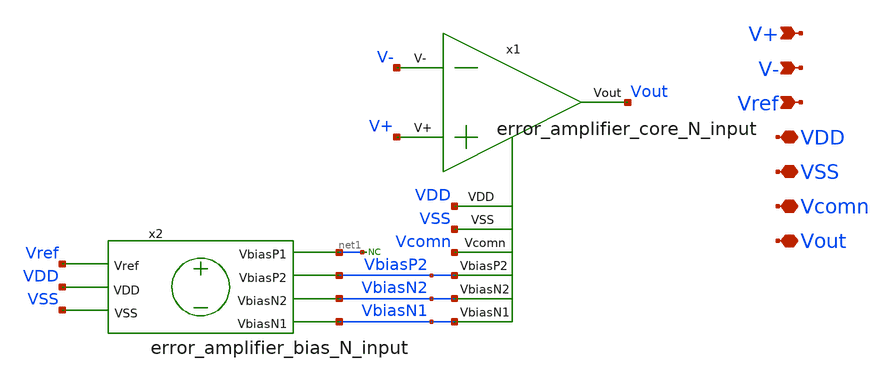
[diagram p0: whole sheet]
** sch_path: blocks/composite/folded_cascode/designs/gf180/error_amplifier_N_input/xschem/error_amplifier_N_input.sch
**.subckt error_amplifier_N_input V+ Vout V- Vref VDD VSS Vcomn
*.ipin V+
*.iopin Vout
*.ipin V-
*.ipin Vref
*.iopin VDD
*.iopin VSS
*.iopin Vcomn
x1 VbiasP2 VbiasN2 VbiasN1 Vout V+ V- VDD VSS Vcomn error_amplifier_core_N_input
x2 VbiasN1 VbiasN2 VbiasP2 VDD VSS Vref net1 error_amplifier_bias_N_input
* noconn #net1
**.ends

* expanding   symbol:  error_amplifier_core_N_input.sym # of pins=9
** sym_path: blocks/composite/folded_cascode/designs/gf180/error_amplifier_core_N_input/xschem/error_amplifier_core_N_input.sym
** sch_path: blocks/composite/folded_cascode/designs/gf180/error_amplifier_core_N_input/xschem/error_amplifier_core_N_input.sch
.subckt error_amplifier_core_N_input VbiasP2 VbiasN2 VbiasN1 Vout V+ V- VDD VSS Vcomn
*.ipin VbiasN2
*.iopin VDD
*.ipin VbiasP2
*.ipin VbiasN1
*.ipin V+
*.ipin V-
*.iopin VSS
*.iopin Vcomn
*.iopin Vout
XM4 Vdm6 Val VDD VDD pfet_03v3 L=0.3u W=4u nf=1 ad='int((nf+1)/2) * W/nf * 0.18u' as='int((nf+2)/2) * W/nf * 0.18u'
+ pd='2*int((nf+1)/2) * (W/nf + 0.18u)' ps='2*int((nf+2)/2) * (W/nf + 0.18u)' nrd='0.18u / W' nrs='0.18u / W'
+ sa=0 sb=0 sd=0 m=12
XM3 Vdm5 Val VDD VDD pfet_03v3 L=0.3u W=4u nf=1 ad='int((nf+1)/2) * W/nf * 0.18u' as='int((nf+2)/2) * W/nf * 0.18u'
+ pd='2*int((nf+1)/2) * (W/nf + 0.18u)' ps='2*int((nf+2)/2) * (W/nf + 0.18u)' nrd='0.18u / W' nrs='0.18u / W'
+ sa=0 sb=0 sd=0 m=12
XM5 Val VbiasP2 Vdm5 VDD pfet_03v3 L=2u W=6u nf=1 ad='int((nf+1)/2) * W/nf * 0.18u' as='int((nf+2)/2) * W/nf * 0.18u'
+ pd='2*int((nf+1)/2) * (W/nf + 0.18u)' ps='2*int((nf+2)/2) * (W/nf + 0.18u)' nrd='0.18u / W' nrs='0.18u / W'
+ sa=0 sb=0 sd=0 m=2
XM6 Vout VbiasP2 Vdm6 VDD pfet_03v3 L=2u W=6u nf=1 ad='int((nf+1)/2) * W/nf * 0.18u' as='int((nf+2)/2) * W/nf * 0.18u'
+ pd='2*int((nf+1)/2) * (W/nf + 0.18u)' ps='2*int((nf+2)/2) * (W/nf + 0.18u)' nrd='0.18u / W' nrs='0.18u / W'
+ sa=0 sb=0 sd=0 m=2
XM9 net1 VbiasN1 VSS VSS nfet_03v3 L=2u W=2u nf=1 ad='int((nf+1)/2) * W/nf * 0.18u' as='int((nf+2)/2) * W/nf * 0.18u'
+ pd='2*int((nf+1)/2) * (W/nf + 0.18u)' ps='2*int((nf+2)/2) * (W/nf + 0.18u)' nrd='0.18u / W' nrs='0.18u / W'
+ sa=0 sb=0 sd=0 m=2
XM8 Vout VbiasN2 Vcomn VSS nfet_03v3 L=2u W=5u nf=1 ad='int((nf+1)/2) * W/nf * 0.18u' as='int((nf+2)/2) * W/nf * 0.18u'
+ pd='2*int((nf+1)/2) * (W/nf + 0.18u)' ps='2*int((nf+2)/2) * (W/nf + 0.18u)' nrd='0.18u / W' nrs='0.18u / W'
+ sa=0 sb=0 sd=0 m=1
XM7 Val VbiasN2 net1 VSS nfet_03v3 L=2u W=5u nf=1 ad='int((nf+1)/2) * W/nf * 0.18u' as='int((nf+2)/2) * W/nf * 0.18u'
+ pd='2*int((nf+1)/2) * (W/nf + 0.18u)' ps='2*int((nf+2)/2) * (W/nf + 0.18u)' nrd='0.18u / W' nrs='0.18u / W'
+ sa=0 sb=0 sd=0 m=1
XM10 Vcomn VbiasN1 VSS VSS nfet_03v3 L=2u W=2u nf=1 ad='int((nf+1)/2) * W/nf * 0.18u' as='int((nf+2)/2) * W/nf * 0.18u'
+ pd='2*int((nf+1)/2) * (W/nf + 0.18u)' ps='2*int((nf+2)/2) * (W/nf + 0.18u)' nrd='0.18u / W' nrs='0.18u / W'
+ sa=0 sb=0 sd=0 m=2
XM15 VDD VDD VDD VDD pfet_03v3 L=3u W=1u nf=1 ad='int((nf+1)/2) * W/nf * 0.18u' as='int((nf+2)/2) * W/nf * 0.18u'
+ pd='2*int((nf+1)/2) * (W/nf + 0.18u)' ps='2*int((nf+2)/2) * (W/nf + 0.18u)' nrd='0.18u / W' nrs='0.18u / W'
+ sa=0 sb=0 sd=0 m=28
XM16 VDD VDD VDD VDD pfet_03v3 L=1.5u W=1u nf=1 ad='int((nf+1)/2) * W/nf * 0.18u' as='int((nf+2)/2) * W/nf * 0.18u'
+ pd='2*int((nf+1)/2) * (W/nf + 0.18u)' ps='2*int((nf+2)/2) * (W/nf + 0.18u)' nrd='0.18u / W' nrs='0.18u / W'
+ sa=0 sb=0 sd=0 m=20
XM13 VSS VSS VSS VSS nfet_03v3 L=3u W=1u nf=1 ad='int((nf+1)/2) * W/nf * 0.18u' as='int((nf+2)/2) * W/nf * 0.18u'
+ pd='2*int((nf+1)/2) * (W/nf + 0.18u)' ps='2*int((nf+2)/2) * (W/nf + 0.18u)' nrd='0.18u / W' nrs='0.18u / W'
+ sa=0 sb=0 sd=0 m=18
XM12 VSS VSS VSS VSS nfet_03v3 L=6.5u W=0.5u nf=1 ad='int((nf+1)/2) * W/nf * 0.18u' as='int((nf+2)/2) * W/nf * 0.18u'
+ pd='2*int((nf+1)/2) * (W/nf + 0.18u)' ps='2*int((nf+2)/2) * (W/nf + 0.18u)' nrd='0.18u / W' nrs='0.18u / W'
+ sa=0 sb=0 sd=0 m=36
XM14 VSS VSS VSS VSS nfet_03v3 L=1u W=1u nf=1 ad='int((nf+1)/2) * W/nf * 0.18u' as='int((nf+2)/2) * W/nf * 0.18u'
+ pd='2*int((nf+1)/2) * (W/nf + 0.18u)' ps='2*int((nf+2)/2) * (W/nf + 0.18u)' nrd='0.18u / W' nrs='0.18u / W'
+ sa=0 sb=0 sd=0 m=30
XM1 Vdm6 V- net2 VSS nfet_03v3 L=1u W=10u nf=1 ad='int((nf+1)/2) * W/nf * 0.18u' as='int((nf+2)/2) * W/nf * 0.18u'
+ pd='2*int((nf+1)/2) * (W/nf + 0.18u)' ps='2*int((nf+2)/2) * (W/nf + 0.18u)' nrd='0.18u / W' nrs='0.18u / W'
+ sa=0 sb=0 sd=0 m=20
XM2 Vdm5 V+ net2 VSS nfet_03v3 L=1u W=10u nf=1 ad='int((nf+1)/2) * W/nf * 0.18u' as='int((nf+2)/2) * W/nf * 0.18u'
+ pd='2*int((nf+1)/2) * (W/nf + 0.18u)' ps='2*int((nf+2)/2) * (W/nf + 0.18u)' nrd='0.18u / W' nrs='0.18u / W'
+ sa=0 sb=0 sd=0 m=20
XM11 net2 VbiasN1 VSS VSS nfet_03v3 L=2u W=2u nf=1 ad='int((nf+1)/2) * W/nf * 0.18u' as='int((nf+2)/2) * W/nf * 0.18u'
+ pd='2*int((nf+1)/2) * (W/nf + 0.18u)' ps='2*int((nf+2)/2) * (W/nf + 0.18u)' nrd='0.18u / W' nrs='0.18u / W'
+ sa=0 sb=0 sd=0 m=40
.ends


* expanding   symbol:  error_amplifier_bias_N_input.sym # of pins=7
** sym_path: blocks/composite/folded_cascode/designs/gf180/error_amplifier_bias_N_input/xschem/error_amplifier_bias_N_input.sym
** sch_path: blocks/composite/folded_cascode/designs/gf180/error_amplifier_bias_N_input/xschem/error_amplifier_bias_N_input.sch
.subckt error_amplifier_bias_N_input VbiasN1 VbiasN2 VbiasP2 VDD VSS Vref VbiasP1
*.ipin Vref
*.iopin VbiasN1
*.iopin VbiasN2
*.iopin VDD
*.iopin VbiasP2
*.iopin VSS
*.iopin VbiasP1
XM1 VbiasN2 VbiasN2 net2 VSS nfet_03v3 L=6u W=0.5u nf=1 ad='int((nf+1)/2) * W/nf * 0.18u' as='int((nf+2)/2) * W/nf * 0.18u'
+ pd='2*int((nf+1)/2) * (W/nf + 0.18u)' ps='2*int((nf+2)/2) * (W/nf + 0.18u)' nrd='0.18u / W' nrs='0.18u / W'
+ sa=0 sb=0 sd=0 m=1
XM2 VbiasP1 VbiasP1 VDD VDD pfet_03v3 L=2u W=0.5u nf=1 ad='int((nf+1)/2) * W/nf * 0.18u' as='int((nf+2)/2) * W/nf * 0.18u'
+ pd='2*int((nf+1)/2) * (W/nf + 0.18u)' ps='2*int((nf+2)/2) * (W/nf + 0.18u)' nrd='0.18u / W' nrs='0.18u / W'
+ sa=0 sb=0 sd=0 m=1
XM3 VbiasP1 Vref net1 VSS nfet_03v3 L=6u W=0.5u nf=1 ad='int((nf+1)/2) * W/nf * 0.18u' as='int((nf+2)/2) * W/nf * 0.18u'
+ pd='2*int((nf+1)/2) * (W/nf + 0.18u)' ps='2*int((nf+2)/2) * (W/nf + 0.18u)' nrd='0.18u / W' nrs='0.18u / W'
+ sa=0 sb=0 sd=0 m=1
XM4 VbiasN2 VbiasP1 VDD VDD pfet_03v3 L=2u W=0.5u nf=1 ad='int((nf+1)/2) * W/nf * 0.18u' as='int((nf+2)/2) * W/nf * 0.18u'
+ pd='2*int((nf+1)/2) * (W/nf + 0.18u)' ps='2*int((nf+2)/2) * (W/nf + 0.18u)' nrd='0.18u / W' nrs='0.18u / W'
+ sa=0 sb=0 sd=0 m=1
XM5 VbiasN1 VbiasP1 VDD VDD pfet_03v3 L=2u W=0.5u nf=1 ad='int((nf+1)/2) * W/nf * 0.18u' as='int((nf+2)/2) * W/nf * 0.18u'
+ pd='2*int((nf+1)/2) * (W/nf + 0.18u)' ps='2*int((nf+2)/2) * (W/nf + 0.18u)' nrd='0.18u / W' nrs='0.18u / W'
+ sa=0 sb=0 sd=0 m=1
XM6 net6 VbiasP2 VDD VDD pfet_03v3 L=2u W=0.5u nf=1 ad='int((nf+1)/2) * W/nf * 0.18u' as='int((nf+2)/2) * W/nf * 0.18u'
+ pd='2*int((nf+1)/2) * (W/nf + 0.18u)' ps='2*int((nf+2)/2) * (W/nf + 0.18u)' nrd='0.18u / W' nrs='0.18u / W'
+ sa=0 sb=0 sd=0 m=1
XM7 VbiasP2 VbiasP2 net6 VDD pfet_03v3 L=2u W=0.5u nf=1 ad='int((nf+1)/2) * W/nf * 0.18u' as='int((nf+2)/2) * W/nf * 0.18u'
+ pd='2*int((nf+1)/2) * (W/nf + 0.18u)' ps='2*int((nf+2)/2) * (W/nf + 0.18u)' nrd='0.18u / W' nrs='0.18u / W'
+ sa=0 sb=0 sd=0 m=1
XM8 net7 net8 VDD VDD pfet_03v3 L=2u W=0.5u nf=1 ad='int((nf+1)/2) * W/nf * 0.18u' as='int((nf+2)/2) * W/nf * 0.18u'
+ pd='2*int((nf+1)/2) * (W/nf + 0.18u)' ps='2*int((nf+2)/2) * (W/nf + 0.18u)' nrd='0.18u / W' nrs='0.18u / W'
+ sa=0 sb=0 sd=0 m=3
XM9 net8 VbiasP2 net7 VDD pfet_03v3 L=2u W=0.5u nf=1 ad='int((nf+1)/2) * W/nf * 0.18u' as='int((nf+2)/2) * W/nf * 0.18u'
+ pd='2*int((nf+1)/2) * (W/nf + 0.18u)' ps='2*int((nf+2)/2) * (W/nf + 0.18u)' nrd='0.18u / W' nrs='0.18u / W'
+ sa=0 sb=0 sd=0 m=2
XM10 net10 VbiasN1 VSS VSS nfet_03v3 L=6u W=0.5u nf=1 ad='int((nf+1)/2) * W/nf * 0.18u' as='int((nf+2)/2) * W/nf * 0.18u'
+ pd='2*int((nf+1)/2) * (W/nf + 0.18u)' ps='2*int((nf+2)/2) * (W/nf + 0.18u)' nrd='0.18u / W' nrs='0.18u / W'
+ sa=0 sb=0 sd=0 m=4
XM11 VbiasN1 VbiasN2 net3 VSS nfet_03v3 L=6u W=0.5u nf=1 ad='int((nf+1)/2) * W/nf * 0.18u' as='int((nf+2)/2) * W/nf * 0.18u'
+ pd='2*int((nf+1)/2) * (W/nf + 0.18u)' ps='2*int((nf+2)/2) * (W/nf + 0.18u)' nrd='0.18u / W' nrs='0.18u / W'
+ sa=0 sb=0 sd=0 m=5
XM12 VbiasP2 VbiasN2 net4 VSS nfet_03v3 L=6u W=0.5u nf=1 ad='int((nf+1)/2) * W/nf * 0.18u' as='int((nf+2)/2) * W/nf * 0.18u'
+ pd='2*int((nf+1)/2) * (W/nf + 0.18u)' ps='2*int((nf+2)/2) * (W/nf + 0.18u)' nrd='0.18u / W' nrs='0.18u / W'
+ sa=0 sb=0 sd=0 m=5
XM13 net8 VbiasN2 net9 VSS nfet_03v3 L=6u W=0.5u nf=1 ad='int((nf+1)/2) * W/nf * 0.18u' as='int((nf+2)/2) * W/nf * 0.18u'
+ pd='2*int((nf+1)/2) * (W/nf + 0.18u)' ps='2*int((nf+2)/2) * (W/nf + 0.18u)' nrd='0.18u / W' nrs='0.18u / W'
+ sa=0 sb=0 sd=0 m=5
XM14 net2 VbiasN2 VSS VSS nfet_03v3 L=6u W=0.5u nf=1 ad='int((nf+1)/2) * W/nf * 0.18u' as='int((nf+2)/2) * W/nf * 0.18u'
+ pd='2*int((nf+1)/2) * (W/nf + 0.18u)' ps='2*int((nf+2)/2) * (W/nf + 0.18u)' nrd='0.18u / W' nrs='0.18u / W'
+ sa=0 sb=0 sd=0 m=1
XM15 net3 VbiasN1 net11 VSS nfet_03v3 L=6u W=0.5u nf=1 ad='int((nf+1)/2) * W/nf * 0.18u' as='int((nf+2)/2) * W/nf * 0.18u'
+ pd='2*int((nf+1)/2) * (W/nf + 0.18u)' ps='2*int((nf+2)/2) * (W/nf + 0.18u)' nrd='0.18u / W' nrs='0.18u / W'
+ sa=0 sb=0 sd=0 m=4
XM16 net4 VbiasN1 net5 VSS nfet_03v3 L=6u W=0.5u nf=1 ad='int((nf+1)/2) * W/nf * 0.18u' as='int((nf+2)/2) * W/nf * 0.18u'
+ pd='2*int((nf+1)/2) * (W/nf + 0.18u)' ps='2*int((nf+2)/2) * (W/nf + 0.18u)' nrd='0.18u / W' nrs='0.18u / W'
+ sa=0 sb=0 sd=0 m=4
XM17 net9 VbiasN1 net10 VSS nfet_03v3 L=6u W=0.5u nf=1 ad='int((nf+1)/2) * W/nf * 0.18u' as='int((nf+2)/2) * W/nf * 0.18u'
+ pd='2*int((nf+1)/2) * (W/nf + 0.18u)' ps='2*int((nf+2)/2) * (W/nf + 0.18u)' nrd='0.18u / W' nrs='0.18u / W'
+ sa=0 sb=0 sd=0 m=4
XM18 net1 Vref VSS VSS nfet_03v3 L=6u W=0.5u nf=1 ad='int((nf+1)/2) * W/nf * 0.18u' as='int((nf+2)/2) * W/nf * 0.18u'
+ pd='2*int((nf+1)/2) * (W/nf + 0.18u)' ps='2*int((nf+2)/2) * (W/nf + 0.18u)' nrd='0.18u / W' nrs='0.18u / W'
+ sa=0 sb=0 sd=0 m=1
XM19 net5 VbiasN1 VSS VSS nfet_03v3 L=6u W=0.5u nf=1 ad='int((nf+1)/2) * W/nf * 0.18u' as='int((nf+2)/2) * W/nf * 0.18u'
+ pd='2*int((nf+1)/2) * (W/nf + 0.18u)' ps='2*int((nf+2)/2) * (W/nf + 0.18u)' nrd='0.18u / W' nrs='0.18u / W'
+ sa=0 sb=0 sd=0 m=4
XM20 net11 VbiasN1 VSS VSS nfet_03v3 L=6u W=0.5u nf=1 ad='int((nf+1)/2) * W/nf * 0.18u' as='int((nf+2)/2) * W/nf * 0.18u'
+ pd='2*int((nf+1)/2) * (W/nf + 0.18u)' ps='2*int((nf+2)/2) * (W/nf + 0.18u)' nrd='0.18u / W' nrs='0.18u / W'
+ sa=0 sb=0 sd=0 m=4
.ends

.end
